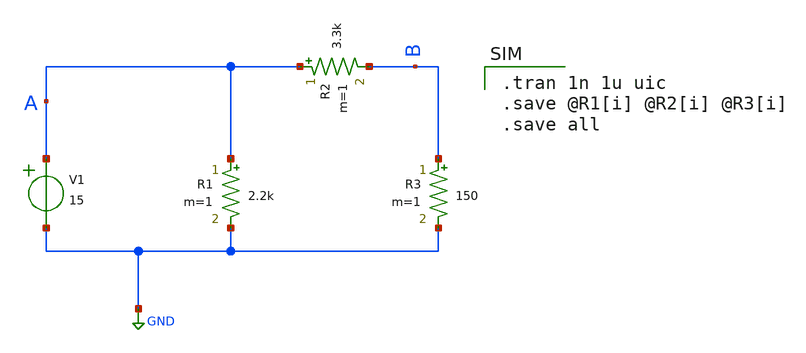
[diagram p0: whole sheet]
** sch_path: lab2.sch
**.subckt lab2
R3 B GND 150 m=1
R2 A B 3.3k m=1
R1 A GND 2.2k m=1
V1 A GND VOL=' 15 '
**** begin user architecture code

.tran 1n 1u uic
.save @R1[i] @R2[i] @R3[i]
.save all

**** end user architecture code
**.ends
.GLOBAL GND
.end
